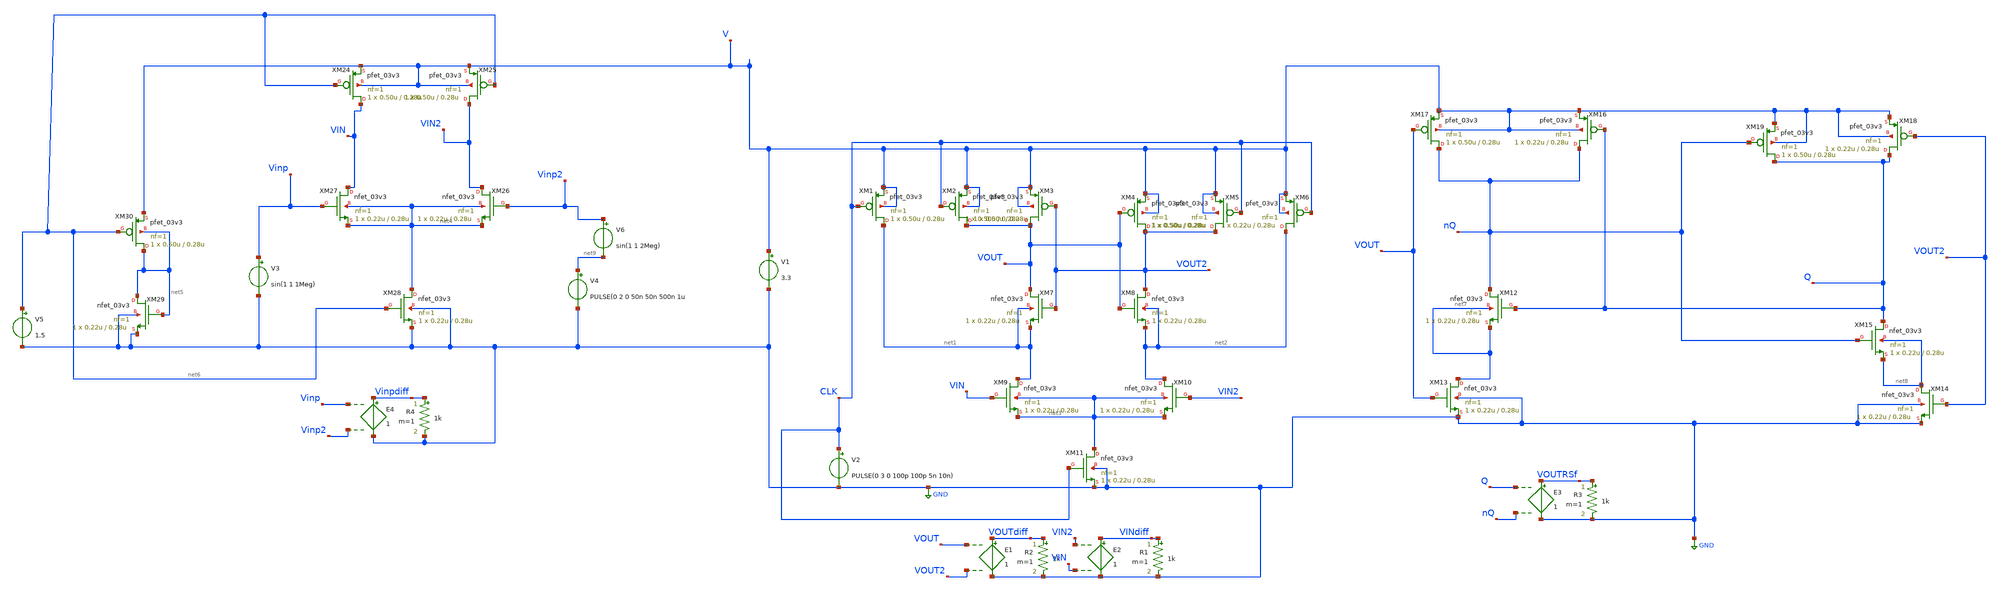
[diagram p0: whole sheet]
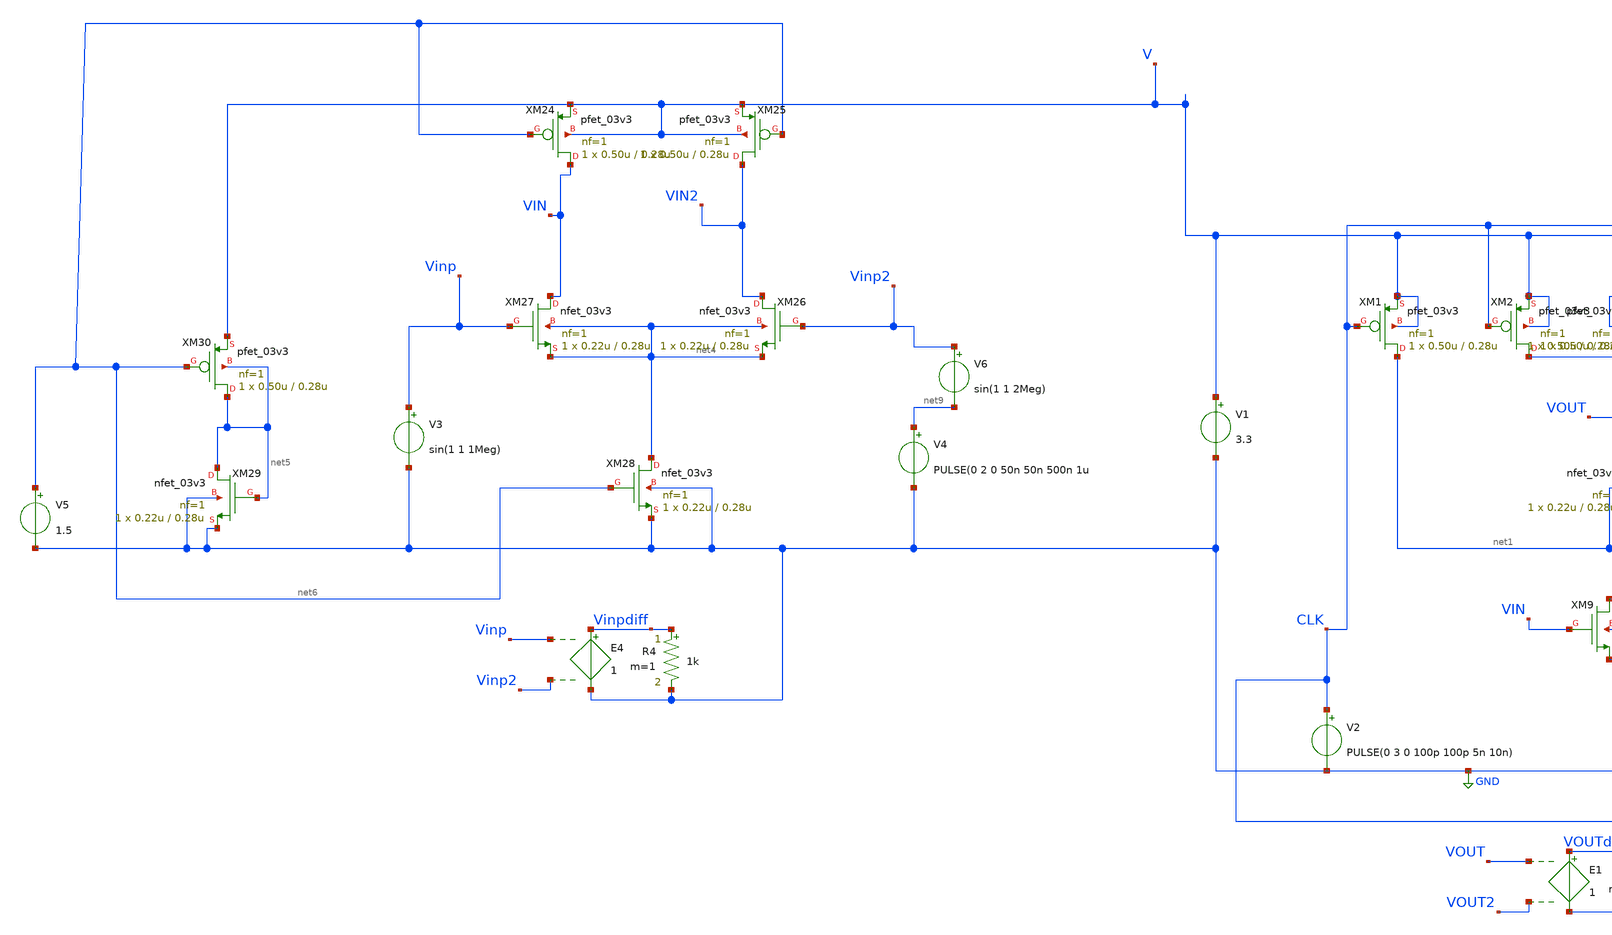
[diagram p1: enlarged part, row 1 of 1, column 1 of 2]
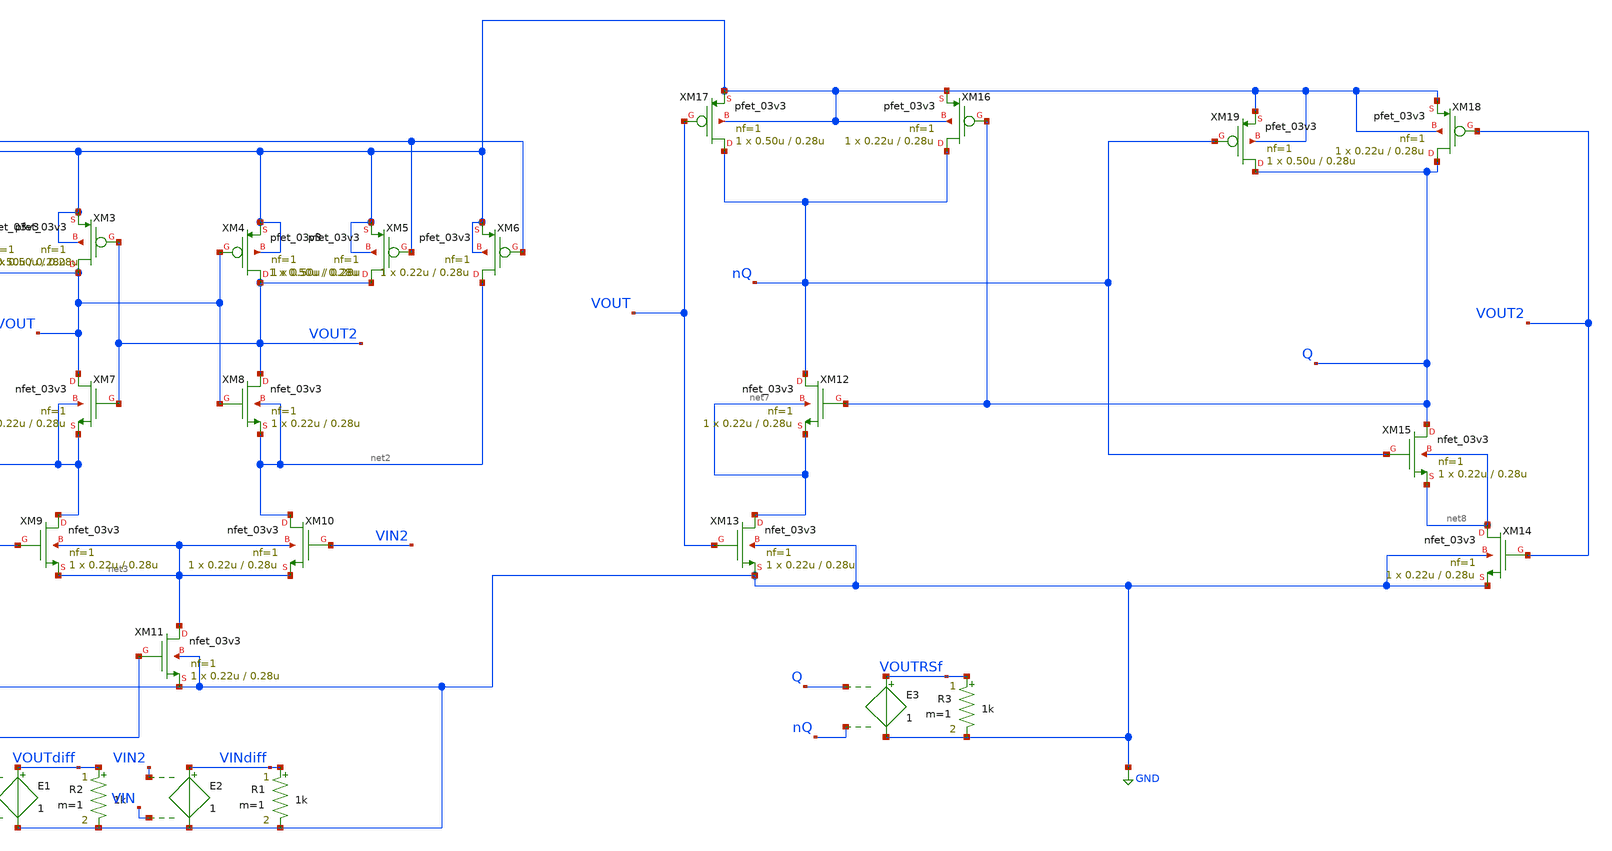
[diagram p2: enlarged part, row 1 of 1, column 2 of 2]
** sch_path: old/StrongArm_nand_latch.sch
**.subckt StrongArm_nand_latch
XM1 net1 CLK V V pfet_03v3 L=0.28u W=0.50u nf=1 ad='int((nf+1)/2) * W/nf * 0.18u' as='int((nf+2)/2) * W/nf * 0.18u'
+ pd='2*int((nf+1)/2) * (W/nf + 0.18u)' ps='2*int((nf+2)/2) * (W/nf + 0.18u)' nrd='0.18u / W' nrs='0.18u / W'
+ sa=0 sb=0 sd=0 m=1
XM2 VOUT CLK V V pfet_03v3 L=0.28u W=0.50u nf=1 ad='int((nf+1)/2) * W/nf * 0.18u' as='int((nf+2)/2) * W/nf * 0.18u'
+ pd='2*int((nf+1)/2) * (W/nf + 0.18u)' ps='2*int((nf+2)/2) * (W/nf + 0.18u)' nrd='0.18u / W' nrs='0.18u / W'
+ sa=0 sb=0 sd=0 m=1
XM3 VOUT VOUT2 V V pfet_03v3 L=0.28u W=0.50u nf=1 ad='int((nf+1)/2) * W/nf * 0.18u' as='int((nf+2)/2) * W/nf * 0.18u'
+ pd='2*int((nf+1)/2) * (W/nf + 0.18u)' ps='2*int((nf+2)/2) * (W/nf + 0.18u)' nrd='0.18u / W' nrs='0.18u / W'
+ sa=0 sb=0 sd=0 m=1
XM4 VOUT2 VOUT V V pfet_03v3 L=0.28u W=0.50u nf=1 ad='int((nf+1)/2) * W/nf * 0.18u' as='int((nf+2)/2) * W/nf * 0.18u'
+ pd='2*int((nf+1)/2) * (W/nf + 0.18u)' ps='2*int((nf+2)/2) * (W/nf + 0.18u)' nrd='0.18u / W' nrs='0.18u / W'
+ sa=0 sb=0 sd=0 m=1
XM5 VOUT2 CLK V V pfet_03v3 L=0.28u W=0.50u nf=1 ad='int((nf+1)/2) * W/nf * 0.18u' as='int((nf+2)/2) * W/nf * 0.18u'
+ pd='2*int((nf+1)/2) * (W/nf + 0.18u)' ps='2*int((nf+2)/2) * (W/nf + 0.18u)' nrd='0.18u / W' nrs='0.18u / W'
+ sa=0 sb=0 sd=0 m=1
XM6 net2 CLK V V pfet_03v3 L=0.28u W=0.22u nf=1 ad='int((nf+1)/2) * W/nf * 0.18u' as='int((nf+2)/2) * W/nf * 0.18u'
+ pd='2*int((nf+1)/2) * (W/nf + 0.18u)' ps='2*int((nf+2)/2) * (W/nf + 0.18u)' nrd='0.18u / W' nrs='0.18u / W'
+ sa=0 sb=0 sd=0 m=1
XM7 VOUT VOUT2 net1 net1 nfet_03v3 L=0.28u W=0.22u nf=1 ad='int((nf+1)/2) * W/nf * 0.18u' as='int((nf+2)/2) * W/nf * 0.18u'
+ pd='2*int((nf+1)/2) * (W/nf + 0.18u)' ps='2*int((nf+2)/2) * (W/nf + 0.18u)' nrd='0.18u / W' nrs='0.18u / W'
+ sa=0 sb=0 sd=0 m=1
XM8 VOUT2 VOUT net2 net2 nfet_03v3 L=0.28u W=0.22u nf=1 ad='int((nf+1)/2) * W/nf * 0.18u' as='int((nf+2)/2) * W/nf * 0.18u'
+ pd='2*int((nf+1)/2) * (W/nf + 0.18u)' ps='2*int((nf+2)/2) * (W/nf + 0.18u)' nrd='0.18u / W' nrs='0.18u / W'
+ sa=0 sb=0 sd=0 m=1
XM9 net1 VIN net3 net3 nfet_03v3 L=0.28u W=0.22u nf=1 ad='int((nf+1)/2) * W/nf * 0.18u' as='int((nf+2)/2) * W/nf * 0.18u'
+ pd='2*int((nf+1)/2) * (W/nf + 0.18u)' ps='2*int((nf+2)/2) * (W/nf + 0.18u)' nrd='0.18u / W' nrs='0.18u / W'
+ sa=0 sb=0 sd=0 m=1
XM10 net2 VIN2 net3 net3 nfet_03v3 L=0.28u W=0.22u nf=1 ad='int((nf+1)/2) * W/nf * 0.18u' as='int((nf+2)/2) * W/nf * 0.18u'
+ pd='2*int((nf+1)/2) * (W/nf + 0.18u)' ps='2*int((nf+2)/2) * (W/nf + 0.18u)' nrd='0.18u / W' nrs='0.18u / W'
+ sa=0 sb=0 sd=0 m=1
XM11 net3 CLK GND GND nfet_03v3 L=0.28u W=0.22u nf=1 ad='int((nf+1)/2) * W/nf * 0.18u' as='int((nf+2)/2) * W/nf * 0.18u'
+ pd='2*int((nf+1)/2) * (W/nf + 0.18u)' ps='2*int((nf+2)/2) * (W/nf + 0.18u)' nrd='0.18u / W' nrs='0.18u / W'
+ sa=0 sb=0 sd=0 m=1
V1 V GND 3.3
V2 CLK GND PULSE(0 3 0 100p 100p 5n 10n)
R2 VOUTdiff GND 1k m=1
E1 VOUTdiff GND VOUT VOUT2 1
R1 VINdiff GND 1k m=1
E2 VINdiff GND VIN2 VIN 1
XM12 nQ Q net7 net7 nfet_03v3 L=0.28u W=0.22u nf=1 ad='int((nf+1)/2) * W/nf * 0.18u' as='int((nf+2)/2) * W/nf * 0.18u'
+ pd='2*int((nf+1)/2) * (W/nf + 0.18u)' ps='2*int((nf+2)/2) * (W/nf + 0.18u)' nrd='0.18u / W' nrs='0.18u / W'
+ sa=0 sb=0 sd=0 m=1
XM13 net7 VOUT GND GND nfet_03v3 L=0.28u W=0.22u nf=1 ad='int((nf+1)/2) * W/nf * 0.18u' as='int((nf+2)/2) * W/nf * 0.18u'
+ pd='2*int((nf+1)/2) * (W/nf + 0.18u)' ps='2*int((nf+2)/2) * (W/nf + 0.18u)' nrd='0.18u / W' nrs='0.18u / W'
+ sa=0 sb=0 sd=0 m=1
XM14 net8 VOUT2 GND GND nfet_03v3 L=0.28u W=0.22u nf=1 ad='int((nf+1)/2) * W/nf * 0.18u' as='int((nf+2)/2) * W/nf * 0.18u'
+ pd='2*int((nf+1)/2) * (W/nf + 0.18u)' ps='2*int((nf+2)/2) * (W/nf + 0.18u)' nrd='0.18u / W' nrs='0.18u / W'
+ sa=0 sb=0 sd=0 m=1
XM15 Q nQ net8 net8 nfet_03v3 L=0.28u W=0.22u nf=1 ad='int((nf+1)/2) * W/nf * 0.18u' as='int((nf+2)/2) * W/nf * 0.18u'
+ pd='2*int((nf+1)/2) * (W/nf + 0.18u)' ps='2*int((nf+2)/2) * (W/nf + 0.18u)' nrd='0.18u / W' nrs='0.18u / W'
+ sa=0 sb=0 sd=0 m=1
XM16 nQ Q V V pfet_03v3 L=0.28u W=0.22u nf=1 ad='int((nf+1)/2) * W/nf * 0.18u' as='int((nf+2)/2) * W/nf * 0.18u'
+ pd='2*int((nf+1)/2) * (W/nf + 0.18u)' ps='2*int((nf+2)/2) * (W/nf + 0.18u)' nrd='0.18u / W' nrs='0.18u / W'
+ sa=0 sb=0 sd=0 m=1
XM17 nQ VOUT V V pfet_03v3 L=0.28u W=0.50u nf=1 ad='int((nf+1)/2) * W/nf * 0.18u' as='int((nf+2)/2) * W/nf * 0.18u'
+ pd='2*int((nf+1)/2) * (W/nf + 0.18u)' ps='2*int((nf+2)/2) * (W/nf + 0.18u)' nrd='0.18u / W' nrs='0.18u / W'
+ sa=0 sb=0 sd=0 m=1
XM18 Q VOUT2 V V pfet_03v3 L=0.28u W=0.22u nf=1 ad='int((nf+1)/2) * W/nf * 0.18u' as='int((nf+2)/2) * W/nf * 0.18u'
+ pd='2*int((nf+1)/2) * (W/nf + 0.18u)' ps='2*int((nf+2)/2) * (W/nf + 0.18u)' nrd='0.18u / W' nrs='0.18u / W'
+ sa=0 sb=0 sd=0 m=1
XM19 Q nQ V V pfet_03v3 L=0.28u W=0.50u nf=1 ad='int((nf+1)/2) * W/nf * 0.18u' as='int((nf+2)/2) * W/nf * 0.18u'
+ pd='2*int((nf+1)/2) * (W/nf + 0.18u)' ps='2*int((nf+2)/2) * (W/nf + 0.18u)' nrd='0.18u / W' nrs='0.18u / W'
+ sa=0 sb=0 sd=0 m=1
R3 VOUTRSf GND 1k m=1
E3 VOUTRSf GND Q nQ 1
XM26 VIN2 Vinp2 net4 net4 nfet_03v3 L=0.28u W=0.22u nf=1 ad='int((nf+1)/2) * W/nf * 0.18u' as='int((nf+2)/2) * W/nf * 0.18u'
+ pd='2*int((nf+1)/2) * (W/nf + 0.18u)' ps='2*int((nf+2)/2) * (W/nf + 0.18u)' nrd='0.18u / W' nrs='0.18u / W'
+ sa=0 sb=0 sd=0 m=1
XM27 VIN Vinp net4 net4 nfet_03v3 L=0.28u W=0.22u nf=1 ad='int((nf+1)/2) * W/nf * 0.18u' as='int((nf+2)/2) * W/nf * 0.18u'
+ pd='2*int((nf+1)/2) * (W/nf + 0.18u)' ps='2*int((nf+2)/2) * (W/nf + 0.18u)' nrd='0.18u / W' nrs='0.18u / W'
+ sa=0 sb=0 sd=0 m=1
V3 Vinp GND sin(1 1 1Meg)
V4 net9 GND PULSE(0 2 0 50n 50n 500n 1u
R4 Vinpdiff GND 1k m=1
E4 Vinpdiff GND Vinp Vinp2 1
XM28 net4 net6 GND GND nfet_03v3 L=0.28u W=0.22u nf=1 ad='int((nf+1)/2) * W/nf * 0.18u' as='int((nf+2)/2) * W/nf * 0.18u'
+ pd='2*int((nf+1)/2) * (W/nf + 0.18u)' ps='2*int((nf+2)/2) * (W/nf + 0.18u)' nrd='0.18u / W' nrs='0.18u / W'
+ sa=0 sb=0 sd=0 m=1
XM29 net5 net5 GND GND nfet_03v3 L=0.28u W=0.22u nf=1 ad='int((nf+1)/2) * W/nf * 0.18u' as='int((nf+2)/2) * W/nf * 0.18u'
+ pd='2*int((nf+1)/2) * (W/nf + 0.18u)' ps='2*int((nf+2)/2) * (W/nf + 0.18u)' nrd='0.18u / W' nrs='0.18u / W'
+ sa=0 sb=0 sd=0 m=1
V5 net6 GND 1.5
XM30 net5 net6 V net5 pfet_03v3 L=0.28u W=0.50u nf=1 ad='int((nf+1)/2) * W/nf * 0.18u' as='int((nf+2)/2) * W/nf * 0.18u'
+ pd='2*int((nf+1)/2) * (W/nf + 0.18u)' ps='2*int((nf+2)/2) * (W/nf + 0.18u)' nrd='0.18u / W' nrs='0.18u / W'
+ sa=0 sb=0 sd=0 m=1
XM24 VIN net6 V V pfet_03v3 L=0.28u W=0.50u nf=1 ad='int((nf+1)/2) * W/nf * 0.18u' as='int((nf+2)/2) * W/nf * 0.18u'
+ pd='2*int((nf+1)/2) * (W/nf + 0.18u)' ps='2*int((nf+2)/2) * (W/nf + 0.18u)' nrd='0.18u / W' nrs='0.18u / W'
+ sa=0 sb=0 sd=0 m=1
XM25 VIN2 net6 V V pfet_03v3 L=0.28u W=0.50u nf=1 ad='int((nf+1)/2) * W/nf * 0.18u' as='int((nf+2)/2) * W/nf * 0.18u'
+ pd='2*int((nf+1)/2) * (W/nf + 0.18u)' ps='2*int((nf+2)/2) * (W/nf + 0.18u)' nrd='0.18u / W' nrs='0.18u / W'
+ sa=0 sb=0 sd=0 m=1
V6 Vinp2 net9 sin(1 1 2Meg)
**** begin user architecture code


.control
save all
tran 100p 10u 30n
plot VOUTrsf Vinpdiff
plot VOUTdiff Vinpdiff
plot VOUTdiff VOUTrsf
plot VOUT VOUT2
.endc


.include /foss/pdks/gf180mcuC/libs.tech/ngspice/design.ngspice
.lib /foss/pdks/gf180mcuC/libs.tech/ngspice/sm141064.ngspice typical

**** end user architecture code
**.ends
.GLOBAL GND
.end
